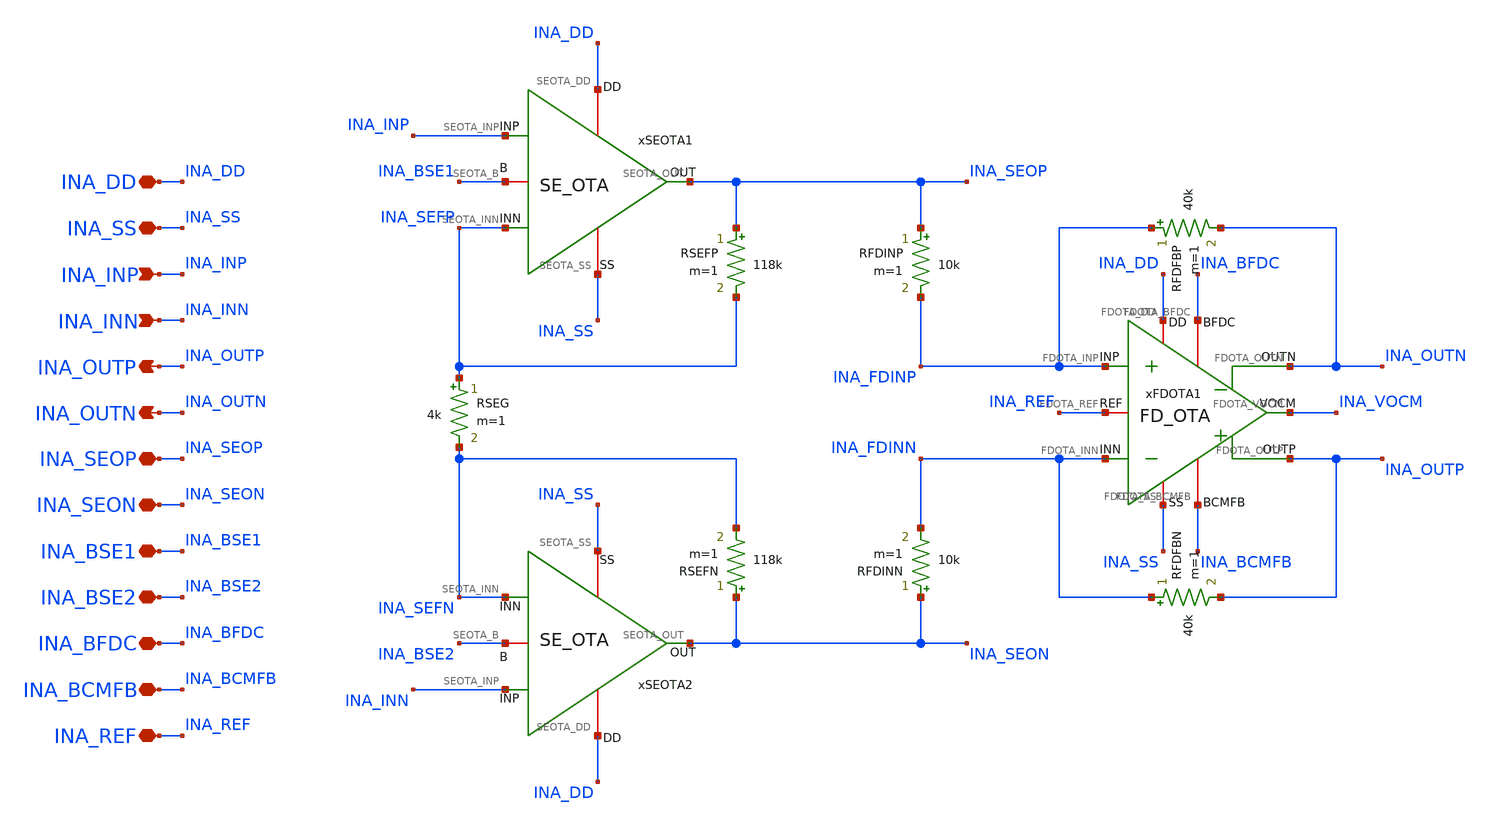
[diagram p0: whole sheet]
** sch_path: Design_Files/IC Design/Schematic/INA/INA.sch
**.subckt INA INA_DD INA_SS INA_INP INA_INN INA_OUTP INA_BFDC INA_OUTN INA_BCMFB INA_REF INA_BSE1
*+ INA_SEON INA_SEOP INA_BSE2
*.iopin INA_DD
*.iopin INA_SS
*.ipin INA_INP
*.ipin INA_INN
*.opin INA_OUTP
*.iopin INA_BFDC
*.opin INA_OUTN
*.iopin INA_BCMFB
*.iopin INA_REF
*.iopin INA_BSE1
*.iopin INA_SEON
*.iopin INA_SEOP
*.iopin INA_BSE2
RFDFBP INA_FDINP INA_OUTN 40k m=1
xFDOTA1 INA_DD INA_SS INA_FDINP INA_FDINN INA_OUTN INA_BFDC INA_OUTP INA_BCMFB INA_REF INA_VOCM
+ FD_OTA
xSEOTA1 INA_DD INA_SS INA_INP INA_SEFP INA_SEOP INA_BSE1 SE_OTA
xSEOTA2 INA_DD INA_SS INA_INN INA_SEFN INA_SEON INA_BSE2 SE_OTA
RFDFBN INA_FDINN INA_OUTP 40k m=1
RFDINP INA_SEOP INA_FDINP 10k m=1
RFDINN INA_SEON INA_FDINN 10k m=1
RSEFP INA_SEOP INA_SEFP 118k m=1
RSEFN INA_SEON INA_SEFN 118k m=1
RSEG INA_SEFP INA_SEFN 4k m=1
**.ends

* expanding   symbol:  ECG_Acquisition_IC/Design_Files/IC Design/Schematic/FD_OTA/FDOTA/FD_OTA.sym #
*+ of pins=10
** sym_path: Design_Files/IC Design/Schematic/FD_OTA/FDOTA/FD_OTA.sym
** sch_path: Design_Files/IC Design/Schematic/FD_OTA/FDOTA/FD_OTA.sch
.subckt FD_OTA FDOTA_DD FDOTA_SS FDOTA_INP FDOTA_INN FDOTA_OUTN FDOTA_BFDC FDOTA_OUTP FDOTA_BCMFB
+ FDOTA_REF FDOTA_VOCM
*.iopin FDOTA_DD
*.iopin FDOTA_SS
*.ipin FDOTA_INP
*.ipin FDOTA_INN
*.opin FDOTA_OUTP
*.iopin FDOTA_BFDC
*.opin FDOTA_OUTN
*.iopin FDOTA_BCMFB
*.iopin FDOTA_REF
*.iopin FDOTA_VOCM
R1 FDOTA_OUTP FDOTA_VOCM 100k m=1
R2 FDOTA_VOCM FDOTA_OUTN 100k m=1
C1 FDOTA_OUTP FDOTA_VOCM 50f m=1
C2 FDOTA_VOCM FDOTA_OUTN 50f m=1
xFDC1 FDOTA_DD FDOTA_SS FDOTA_INP FDOTA_INN FDOTA_OUTN FDOTA_BFDC FDOTA_OUTP FDOTA_VCMFB FDC
xCMFB1 FDOTA_DD FDOTA_SS FDOTA_VOCM FDOTA_REF FDOTA_VCMFB FDOTA_BCMFB CMFB
.ends


* expanding   symbol:  ECG_Acquisition_IC/Design_Files/IC Design/Schematic/SE_OTA/SE_OTA.sym # of
*+ pins=6
** sym_path: Design_Files/IC Design/Schematic/SE_OTA/SE_OTA.sym
** sch_path: Design_Files/IC Design/Schematic/SE_OTA/SE_OTA.sch
.subckt SE_OTA SEOTA_DD SEOTA_SS SEOTA_INP SEOTA_INN SEOTA_OUT SEOTA_B
*.iopin SEOTA_DD
*.iopin SEOTA_SS
*.ipin SEOTA_INP
*.ipin SEOTA_INN
*.opin SEOTA_OUT
*.iopin SEOTA_B
XM3 net4 net4 SEOTA_DD SEOTA_DD pfet_03v3 L=4u W=1u nf=1 ad='int((nf+1)/2) * W/nf * 0.18u' as='int((nf+2)/2) * W/nf * 0.18u'
+ pd='2*int((nf+1)/2) * (W/nf + 0.18u)' ps='2*int((nf+2)/2) * (W/nf + 0.18u)' nrd='0.18u / W' nrs='0.18u / W'
+ sa=0 sb=0 sd=0 m=60
XM7 SEOTA_OUT SEOTA_B SEOTA_SS SEOTA_SS nfet_03v3 L=0.5u W=1u nf=1 ad='int((nf+1)/2) * W/nf * 0.18u'
+ as='int((nf+2)/2) * W/nf * 0.18u' pd='2*int((nf+1)/2) * (W/nf + 0.18u)' ps='2*int((nf+2)/2) * (W/nf + 0.18u)'
+ nrd='0.18u / W' nrs='0.18u / W' sa=0 sb=0 sd=0 m=100
Rz net1 net2 3.8k m=1
XM5 net3 SEOTA_B SEOTA_SS SEOTA_SS nfet_03v3 L=2u W=1u nf=1 ad='int((nf+1)/2) * W/nf * 0.18u' as='int((nf+2)/2) * W/nf * 0.18u'
+ pd='2*int((nf+1)/2) * (W/nf + 0.18u)' ps='2*int((nf+2)/2) * (W/nf + 0.18u)' nrd='0.18u / W' nrs='0.18u / W'
+ sa=0 sb=0 sd=0 m=10
XM6 SEOTA_OUT net1 SEOTA_DD SEOTA_DD pfet_03v3 L=0.5u W=1u nf=1 ad='int((nf+1)/2) * W/nf * 0.18u' as='int((nf+2)/2) * W/nf * 0.18u'
+ pd='2*int((nf+1)/2) * (W/nf + 0.18u)' ps='2*int((nf+2)/2) * (W/nf + 0.18u)' nrd='0.18u / W' nrs='0.18u / W'
+ sa=0 sb=0 sd=0 m=400
XM8 SEOTA_B SEOTA_B SEOTA_SS SEOTA_SS nfet_03v3 L=2u W=1u nf=1 ad='int((nf+1)/2) * W/nf * 0.18u' as='int((nf+2)/2) * W/nf * 0.18u'
+ pd='2*int((nf+1)/2) * (W/nf + 0.18u)' ps='2*int((nf+2)/2) * (W/nf + 0.18u)' nrd='0.18u / W' nrs='0.18u / W'
+ sa=0 sb=0 sd=0 m=20
Cc net2 SEOTA_OUT 2p m=1
XM4 net1 net4 SEOTA_DD SEOTA_DD pfet_03v3 L=4u W=1u nf=1 ad='int((nf+1)/2) * W/nf * 0.18u' as='int((nf+2)/2) * W/nf * 0.18u'
+ pd='2*int((nf+1)/2) * (W/nf + 0.18u)' ps='2*int((nf+2)/2) * (W/nf + 0.18u)' nrd='0.18u / W' nrs='0.18u / W'
+ sa=0 sb=0 sd=0 m=60
XM1 net4 SEOTA_INN net3 SEOTA_SS nfet_03v3 L=4u W=1u nf=1 ad='int((nf+1)/2) * W/nf * 0.18u' as='int((nf+2)/2) * W/nf * 0.18u'
+ pd='2*int((nf+1)/2) * (W/nf + 0.18u)' ps='2*int((nf+2)/2) * (W/nf + 0.18u)' nrd='0.18u / W' nrs='0.18u / W'
+ sa=0 sb=0 sd=0 m=400
XM2 net1 SEOTA_INP net3 SEOTA_SS nfet_03v3 L=4u W=1u nf=1 ad='int((nf+1)/2) * W/nf * 0.18u' as='int((nf+2)/2) * W/nf * 0.18u'
+ pd='2*int((nf+1)/2) * (W/nf + 0.18u)' ps='2*int((nf+2)/2) * (W/nf + 0.18u)' nrd='0.18u / W' nrs='0.18u / W'
+ sa=0 sb=0 sd=0 m=400
.ends


* expanding   symbol:  ECG_Acquisition_IC/Design_Files/IC Design/Schematic/FD_OTA/FDC/FDC.sym # of
*+ pins=8
** sym_path: Design_Files/IC Design/Schematic/FD_OTA/FDC/FDC.sym
** sch_path: Design_Files/IC Design/Schematic/FD_OTA/FDC/FDC.sch
.subckt FDC FDC_DD FDC_SS FDC_INP FDC_INN FDC_OUTN FDC_B FDC_OUTP FDC_CMFB
*.iopin FDC_DD
*.iopin FDC_SS
*.ipin FDC_INP
*.ipin FDC_INN
*.opin FDC_OUTP
*.iopin FDC_B
*.opin FDC_OUTN
*.iopin FDC_CMFB
XM3 net4 FDC_CMFB FDC_DD FDC_DD pfet_03v3 L=2u W=1u nf=1 ad='int((nf+1)/2) * W/nf * 0.18u' as='int((nf+2)/2) * W/nf * 0.18u'
+ pd='2*int((nf+1)/2) * (W/nf + 0.18u)' ps='2*int((nf+2)/2) * (W/nf + 0.18u)' nrd='0.18u / W' nrs='0.18u / W'
+ sa=0 sb=0 sd=0 m=200
XM8 FDC_OUTP FDC_B FDC_SS FDC_SS nfet_03v3 L=0.5u W=1u nf=1 ad='int((nf+1)/2) * W/nf * 0.18u' as='int((nf+2)/2) * W/nf * 0.18u'
+ pd='2*int((nf+1)/2) * (W/nf + 0.18u)' ps='2*int((nf+2)/2) * (W/nf + 0.18u)' nrd='0.18u / W' nrs='0.18u / W'
+ sa=0 sb=0 sd=0 m=100
Rz net1 net2 3.5k m=1
XM5 net3 FDC_B FDC_SS FDC_SS nfet_03v3 L=2u W=1u nf=1 ad='int((nf+1)/2) * W/nf * 0.18u' as='int((nf+2)/2) * W/nf * 0.18u'
+ pd='2*int((nf+1)/2) * (W/nf + 0.18u)' ps='2*int((nf+2)/2) * (W/nf + 0.18u)' nrd='0.18u / W' nrs='0.18u / W'
+ sa=0 sb=0 sd=0 m=10
XM6 FDC_OUTP net1 FDC_DD FDC_DD pfet_03v3 L=0.5u W=1u nf=1 ad='int((nf+1)/2) * W/nf * 0.18u' as='int((nf+2)/2) * W/nf * 0.18u'
+ pd='2*int((nf+1)/2) * (W/nf + 0.18u)' ps='2*int((nf+2)/2) * (W/nf + 0.18u)' nrd='0.18u / W' nrs='0.18u / W'
+ sa=0 sb=0 sd=0 m=200
XM10 FDC_B FDC_B FDC_SS FDC_SS nfet_03v3 L=2u W=1u nf=1 ad='int((nf+1)/2) * W/nf * 0.18u' as='int((nf+2)/2) * W/nf * 0.18u'
+ pd='2*int((nf+1)/2) * (W/nf + 0.18u)' ps='2*int((nf+2)/2) * (W/nf + 0.18u)' nrd='0.18u / W' nrs='0.18u / W'
+ sa=0 sb=0 sd=0 m=20
Cc net2 FDC_OUTP 2.5p m=1
XM9 FDC_OUTN FDC_B FDC_SS FDC_SS nfet_03v3 L=0.5u W=1u nf=1 ad='int((nf+1)/2) * W/nf * 0.18u' as='int((nf+2)/2) * W/nf * 0.18u'
+ pd='2*int((nf+1)/2) * (W/nf + 0.18u)' ps='2*int((nf+2)/2) * (W/nf + 0.18u)' nrd='0.18u / W' nrs='0.18u / W'
+ sa=0 sb=0 sd=0 m=100
Rz1 net4 net5 3.5k m=1
XM7 FDC_OUTN net4 FDC_DD FDC_DD pfet_03v3 L=0.5u W=1u nf=1 ad='int((nf+1)/2) * W/nf * 0.18u' as='int((nf+2)/2) * W/nf * 0.18u'
+ pd='2*int((nf+1)/2) * (W/nf + 0.18u)' ps='2*int((nf+2)/2) * (W/nf + 0.18u)' nrd='0.18u / W' nrs='0.18u / W'
+ sa=0 sb=0 sd=0 m=200
Cc1 net5 FDC_OUTN 2.5p m=1
XM4 net1 FDC_CMFB FDC_DD FDC_DD pfet_03v3 L=2u W=1u nf=1 ad='int((nf+1)/2) * W/nf * 0.18u' as='int((nf+2)/2) * W/nf * 0.18u'
+ pd='2*int((nf+1)/2) * (W/nf + 0.18u)' ps='2*int((nf+2)/2) * (W/nf + 0.18u)' nrd='0.18u / W' nrs='0.18u / W'
+ sa=0 sb=0 sd=0 m=200
XM1 net4 FDC_INN net3 FDC_SS nfet_03v3 L=2u W=1u nf=1 ad='int((nf+1)/2) * W/nf * 0.18u' as='int((nf+2)/2) * W/nf * 0.18u'
+ pd='2*int((nf+1)/2) * (W/nf + 0.18u)' ps='2*int((nf+2)/2) * (W/nf + 0.18u)' nrd='0.18u / W' nrs='0.18u / W'
+ sa=0 sb=0 sd=0 m=200
XM2 net1 FDC_INP net3 FDC_SS nfet_03v3 L=2u W=1u nf=1 ad='int((nf+1)/2) * W/nf * 0.18u' as='int((nf+2)/2) * W/nf * 0.18u'
+ pd='2*int((nf+1)/2) * (W/nf + 0.18u)' ps='2*int((nf+2)/2) * (W/nf + 0.18u)' nrd='0.18u / W' nrs='0.18u / W'
+ sa=0 sb=0 sd=0 m=200
.ends


* expanding   symbol:  ECG_Acquisition_IC/Design_Files/IC Design/Schematic/FD_OTA/CMFB/CMFB.sym # of
*+ pins=6
** sym_path: Design_Files/IC Design/Schematic/FD_OTA/CMFB/CMFB.sym
** sch_path: Design_Files/IC Design/Schematic/FD_OTA/CMFB/CMFB.sch
.subckt CMFB CMFB_DD CMFB_SS CMFB_IN CMFB_REF CMFB_OUT CMFB_B
*.iopin CMFB_DD
*.iopin CMFB_SS
*.ipin CMFB_IN
*.ipin CMFB_REF
*.opin CMFB_OUT
*.iopin CMFB_B
XM4 CMFB_OUT CMFB_OUT CMFB_DD CMFB_DD pfet_03v3 L=0.5u W=1u nf=1 ad='int((nf+1)/2) * W/nf * 0.18u' as='int((nf+2)/2) * W/nf * 0.18u'
+ pd='2*int((nf+1)/2) * (W/nf + 0.18u)' ps='2*int((nf+2)/2) * (W/nf + 0.18u)' nrd='0.18u / W' nrs='0.18u / W'
+ sa=0 sb=0 sd=0 m=77
XM3 net2 net2 CMFB_DD CMFB_DD pfet_03v3 L=0.5u W=1u nf=1 ad='int((nf+1)/2) * W/nf * 0.18u' as='int((nf+2)/2) * W/nf * 0.18u'
+ pd='2*int((nf+1)/2) * (W/nf + 0.18u)' ps='2*int((nf+2)/2) * (W/nf + 0.18u)' nrd='0.18u / W' nrs='0.18u / W'
+ sa=0 sb=0 sd=0 m=77
XM1 net2 CMFB_REF net1 CMFB_SS nfet_03v3 L=0.5u W=1u nf=1 ad='int((nf+1)/2) * W/nf * 0.18u' as='int((nf+2)/2) * W/nf * 0.18u'
+ pd='2*int((nf+1)/2) * (W/nf + 0.18u)' ps='2*int((nf+2)/2) * (W/nf + 0.18u)' nrd='0.18u / W' nrs='0.18u / W'
+ sa=0 sb=0 sd=0 m=5
XM2 CMFB_OUT CMFB_IN net1 CMFB_SS nfet_03v3 L=0.5u W=1u nf=1 ad='int((nf+1)/2) * W/nf * 0.18u' as='int((nf+2)/2) * W/nf * 0.18u'
+ pd='2*int((nf+1)/2) * (W/nf + 0.18u)' ps='2*int((nf+2)/2) * (W/nf + 0.18u)' nrd='0.18u / W' nrs='0.18u / W'
+ sa=0 sb=0 sd=0 m=5
XM5 net1 CMFB_B CMFB_SS CMFB_SS nfet_03v3 L=2u W=1u nf=1 ad='int((nf+1)/2) * W/nf * 0.18u' as='int((nf+2)/2) * W/nf * 0.18u'
+ pd='2*int((nf+1)/2) * (W/nf + 0.18u)' ps='2*int((nf+2)/2) * (W/nf + 0.18u)' nrd='0.18u / W' nrs='0.18u / W'
+ sa=0 sb=0 sd=0 m=20
XM10 CMFB_B CMFB_B CMFB_SS CMFB_SS nfet_03v3 L=2u W=1u nf=1 ad='int((nf+1)/2) * W/nf * 0.18u' as='int((nf+2)/2) * W/nf * 0.18u'
+ pd='2*int((nf+1)/2) * (W/nf + 0.18u)' ps='2*int((nf+2)/2) * (W/nf + 0.18u)' nrd='0.18u / W' nrs='0.18u / W'
+ sa=0 sb=0 sd=0 m=20
.ends

.end
